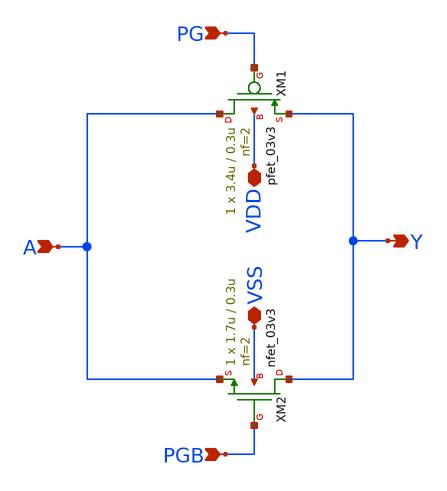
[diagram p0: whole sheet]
** sch_path: xschem/TG.sch
**.subckt TG A Y PG PGB VDD VSS
*.ipin A
*.opin Y
*.ipin PG
*.ipin PGB
*.iopin VDD
*.iopin VSS
XM1 A PG Y VDD pfet_03v3 L=0.3u W=3.4u nf=2 ad='int((nf+1)/2) * W/nf * 0.18u' as='int((nf+2)/2) * W/nf * 0.18u'
+ pd='2*int((nf+1)/2) * (W/nf + 0.18u)' ps='2*int((nf+2)/2) * (W/nf + 0.18u)' nrd='0.18u / W' nrs='0.18u / W'
+ sa=0 sb=0 sd=0 m=1
XM2 Y PGB A VSS nfet_03v3 L=0.3u W=1.7u nf=2 ad='int((nf+1)/2) * W/nf * 0.18u' as='int((nf+2)/2) * W/nf * 0.18u'
+ pd='2*int((nf+1)/2) * (W/nf + 0.18u)' ps='2*int((nf+2)/2) * (W/nf + 0.18u)' nrd='0.18u / W' nrs='0.18u / W'
+ sa=0 sb=0 sd=0 m=1
**.ends
.end
